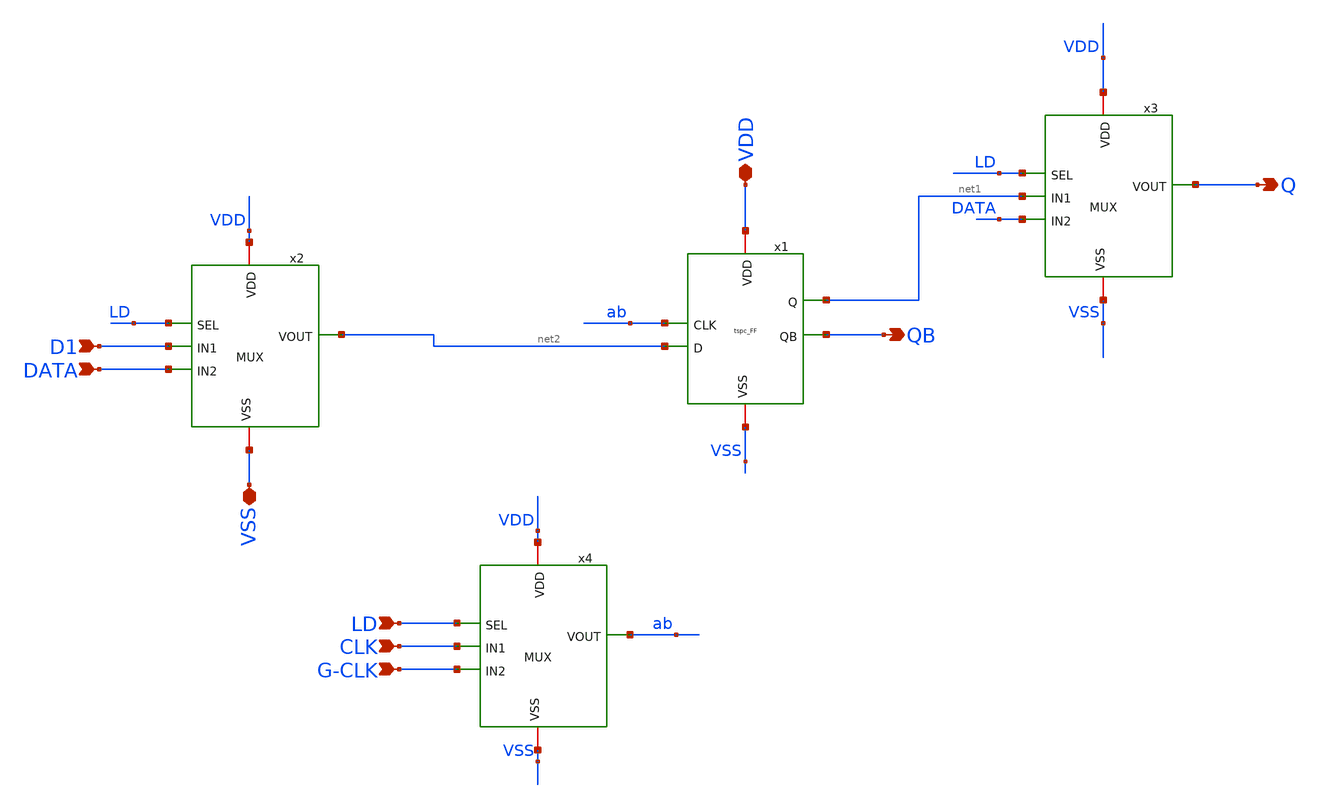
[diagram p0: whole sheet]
** sch_path: PLL-main/schematic/xschem/MOD_DFF_latest.sch
**.subckt MOD_DFF_latest VDD LD VSS D1 CLK G-CLK Q QB DATA
*.iopin VDD
*.ipin LD
*.iopin VSS
*.ipin D1
*.ipin CLK
*.ipin G-CLK
*.opin Q
*.opin QB
*.ipin DATA
x1 VDD QB net1 ab net2 VSS tspc_FF
x2 VDD LD D1 net2 VSS DATA MUX
x3 VDD LD net1 Q VSS DATA MUX
x4 VDD LD CLK ab VSS G-CLK MUX
**.ends

* expanding   symbol:  tspc_FF.sym # of pins=6
** sym_path: tspc_FF.sym
** sch_path: tspc_FF.sch
.subckt tspc_FF VDD QB Q CLK D VSS
*.ipin D
*.ipin CLK
*.iopin VDD
*.iopin VSS
*.opin QB
*.opin Q
XM1 net1 D VSS VSS nfet_03v3 L=0.56u W=1.12u nf=1 ad='int((nf+1)/2) * W/nf * 0.18u' as='int((nf+2)/2) * W/nf * 0.18u'
+ pd='2*int((nf+1)/2) * (W/nf + 0.18u)' ps='2*int((nf+2)/2) * (W/nf + 0.18u)' nrd='0.18u / W' nrs='0.18u / W'
+ sa=0 sb=0 sd=0 m=1
XM2 net1 CLK net2 VDD pfet_03v3 L=0.56u W=4.48u nf=1 ad='int((nf+1)/2) * W/nf * 0.18u' as='int((nf+2)/2) * W/nf * 0.18u'
+ pd='2*int((nf+1)/2) * (W/nf + 0.18u)' ps='2*int((nf+2)/2) * (W/nf + 0.18u)' nrd='0.18u / W' nrs='0.18u / W'
+ sa=0 sb=0 sd=0 m=1
XM3 net2 D VDD VDD pfet_03v3 L=0.56u W=4.48u nf=1 ad='int((nf+1)/2) * W/nf * 0.18u' as='int((nf+2)/2) * W/nf * 0.18u'
+ pd='2*int((nf+1)/2) * (W/nf + 0.18u)' ps='2*int((nf+2)/2) * (W/nf + 0.18u)' nrd='0.18u / W' nrs='0.18u / W'
+ sa=0 sb=0 sd=0 m=1
XM4 net3 CLK VDD VDD pfet_03v3 L=0.56u W=2.24u nf=1 ad='int((nf+1)/2) * W/nf * 0.18u' as='int((nf+2)/2) * W/nf * 0.18u'
+ pd='2*int((nf+1)/2) * (W/nf + 0.18u)' ps='2*int((nf+2)/2) * (W/nf + 0.18u)' nrd='0.18u / W' nrs='0.18u / W'
+ sa=0 sb=0 sd=0 m=1
XM5 net3 net1 net4 VSS nfet_03v3 L=0.56u W=2.24u nf=1 ad='int((nf+1)/2) * W/nf * 0.18u' as='int((nf+2)/2) * W/nf * 0.18u'
+ pd='2*int((nf+1)/2) * (W/nf + 0.18u)' ps='2*int((nf+2)/2) * (W/nf + 0.18u)' nrd='0.18u / W' nrs='0.18u / W'
+ sa=0 sb=0 sd=0 m=1
XM6 net4 CLK VSS VSS nfet_03v3 L=0.56u W=2.24u nf=1 ad='int((nf+1)/2) * W/nf * 0.18u' as='int((nf+2)/2) * W/nf * 0.18u'
+ pd='2*int((nf+1)/2) * (W/nf + 0.18u)' ps='2*int((nf+2)/2) * (W/nf + 0.18u)' nrd='0.18u / W' nrs='0.18u / W'
+ sa=0 sb=0 sd=0 m=1
XM7 QB net3 VDD VDD pfet_03v3 L=0.56u W=2.24u nf=1 ad='int((nf+1)/2) * W/nf * 0.18u' as='int((nf+2)/2) * W/nf * 0.18u'
+ pd='2*int((nf+1)/2) * (W/nf + 0.18u)' ps='2*int((nf+2)/2) * (W/nf + 0.18u)' nrd='0.18u / W' nrs='0.18u / W'
+ sa=0 sb=0 sd=0 m=1
XM8 QB CLK net5 VSS nfet_03v3 L=0.56u W=2.24u nf=1 ad='int((nf+1)/2) * W/nf * 0.18u' as='int((nf+2)/2) * W/nf * 0.18u'
+ pd='2*int((nf+1)/2) * (W/nf + 0.18u)' ps='2*int((nf+2)/2) * (W/nf + 0.18u)' nrd='0.18u / W' nrs='0.18u / W'
+ sa=0 sb=0 sd=0 m=1
XM9 net5 net3 VSS VSS nfet_03v3 L=0.56u W=2.24u nf=1 ad='int((nf+1)/2) * W/nf * 0.18u' as='int((nf+2)/2) * W/nf * 0.18u'
+ pd='2*int((nf+1)/2) * (W/nf + 0.18u)' ps='2*int((nf+2)/2) * (W/nf + 0.18u)' nrd='0.18u / W' nrs='0.18u / W'
+ sa=0 sb=0 sd=0 m=1
XM10 Q QB VDD VDD pfet_03v3 L=0.56u W=2.24u nf=1 ad='int((nf+1)/2) * W/nf * 0.18u' as='int((nf+2)/2) * W/nf * 0.18u'
+ pd='2*int((nf+1)/2) * (W/nf + 0.18u)' ps='2*int((nf+2)/2) * (W/nf + 0.18u)' nrd='0.18u / W' nrs='0.18u / W'
+ sa=0 sb=0 sd=0 m=1
XM11 Q QB VSS VSS nfet_03v3 L=0.56u W=1.12u nf=1 ad='int((nf+1)/2) * W/nf * 0.18u' as='int((nf+2)/2) * W/nf * 0.18u'
+ pd='2*int((nf+1)/2) * (W/nf + 0.18u)' ps='2*int((nf+2)/2) * (W/nf + 0.18u)' nrd='0.18u / W' nrs='0.18u / W'
+ sa=0 sb=0 sd=0 m=1
.ends


* expanding   symbol:  MUX.sym # of pins=6
** sym_path: MUX.sym
** sch_path: MUX.sch
.subckt MUX VDD SEL IN1 VOUT VSS IN2
*.ipin SEL
*.ipin IN1
*.ipin IN2
*.opin VOUT
*.iopin VDD
*.iopin VSS
x2 VDD net3 net1 IN1 VSS AND
x3 VDD net2 SEL IN2 VSS AND
XM4 net1 SEL VDD VDD pfet_03v3 L=0.56u W=6.72u nf=1 ad='int((nf+1)/2) * W/nf * 0.18u' as='int((nf+2)/2) * W/nf * 0.18u'
+ pd='2*int((nf+1)/2) * (W/nf + 0.18u)' ps='2*int((nf+2)/2) * (W/nf + 0.18u)' nrd='0.18u / W' nrs='0.18u / W'
+ sa=0 sb=0 sd=0 m=1
XM5 net1 SEL VSS VSS nfet_03v3 L=0.56u W=3.36u nf=1 ad='int((nf+1)/2) * W/nf * 0.18u' as='int((nf+2)/2) * W/nf * 0.18u'
+ pd='2*int((nf+1)/2) * (W/nf + 0.18u)' ps='2*int((nf+2)/2) * (W/nf + 0.18u)' nrd='0.18u / W' nrs='0.18u / W'
+ sa=0 sb=0 sd=0 m=1
x1 VDD net3 net2 VOUT VSS OR
.ends


* expanding   symbol:  AND.sym # of pins=5
** sym_path: AND.sym
** sch_path: AND.sch
.subckt AND VDD VOUT A B VSS
*.iopin VDD
*.iopin VSS
*.ipin A
*.ipin B
*.opin VOUT
XM1 net1 A net2 VSS nfet_03v3 L=0.56u W=2.24u nf=1 ad='int((nf+1)/2) * W/nf * 0.18u' as='int((nf+2)/2) * W/nf * 0.18u'
+ pd='2*int((nf+1)/2) * (W/nf + 0.18u)' ps='2*int((nf+2)/2) * (W/nf + 0.18u)' nrd='0.18u / W' nrs='0.18u / W'
+ sa=0 sb=0 sd=0 m=1
XM2 net1 A VDD VDD pfet_03v3 L=0.56u W=2.24u nf=1 ad='int((nf+1)/2) * W/nf * 0.18u' as='int((nf+2)/2) * W/nf * 0.18u'
+ pd='2*int((nf+1)/2) * (W/nf + 0.18u)' ps='2*int((nf+2)/2) * (W/nf + 0.18u)' nrd='0.18u / W' nrs='0.18u / W'
+ sa=0 sb=0 sd=0 m=1
XM3 net1 B VDD VDD pfet_03v3 L=0.56u W=2.24u nf=1 ad='int((nf+1)/2) * W/nf * 0.18u' as='int((nf+2)/2) * W/nf * 0.18u'
+ pd='2*int((nf+1)/2) * (W/nf + 0.18u)' ps='2*int((nf+2)/2) * (W/nf + 0.18u)' nrd='0.18u / W' nrs='0.18u / W'
+ sa=0 sb=0 sd=0 m=1
XM4 net2 B VSS VSS nfet_03v3 L=0.56u W=2.24u nf=1 ad='int((nf+1)/2) * W/nf * 0.18u' as='int((nf+2)/2) * W/nf * 0.18u'
+ pd='2*int((nf+1)/2) * (W/nf + 0.18u)' ps='2*int((nf+2)/2) * (W/nf + 0.18u)' nrd='0.18u / W' nrs='0.18u / W'
+ sa=0 sb=0 sd=0 m=1
XM5 VOUT net1 VDD VDD pfet_03v3 L=0.56u W=2.24u nf=1 ad='int((nf+1)/2) * W/nf * 0.18u' as='int((nf+2)/2) * W/nf * 0.18u'
+ pd='2*int((nf+1)/2) * (W/nf + 0.18u)' ps='2*int((nf+2)/2) * (W/nf + 0.18u)' nrd='0.18u / W' nrs='0.18u / W'
+ sa=0 sb=0 sd=0 m=1
XM6 VOUT net1 VSS VSS nfet_03v3 L=0.56u W=1.12u nf=1 ad='int((nf+1)/2) * W/nf * 0.18u' as='int((nf+2)/2) * W/nf * 0.18u'
+ pd='2*int((nf+1)/2) * (W/nf + 0.18u)' ps='2*int((nf+2)/2) * (W/nf + 0.18u)' nrd='0.18u / W' nrs='0.18u / W'
+ sa=0 sb=0 sd=0 m=1
.ends


* expanding   symbol:  OR.sym # of pins=5
** sym_path: PLL-main/schematic/xschem/OR.sym
** sch_path: PLL-main/schematic/xschem/OR.sch
.subckt OR VDD A B VOUT VSS
*.iopin VSS
*.iopin VDD
*.ipin A
*.ipin B
*.opin VOUT
XM1 net1 A VSS VSS nfet_03v3 L=0.56u W=1.12u nf=1 ad='int((nf+1)/2) * W/nf * 0.18u' as='int((nf+2)/2) * W/nf * 0.18u'
+ pd='2*int((nf+1)/2) * (W/nf + 0.18u)' ps='2*int((nf+2)/2) * (W/nf + 0.18u)' nrd='0.18u / W' nrs='0.18u / W'
+ sa=0 sb=0 sd=0 m=1
XM2 net1 B net2 VDD pfet_03v3 L=0.56u W=4.48u nf=1 ad='int((nf+1)/2) * W/nf * 0.18u' as='int((nf+2)/2) * W/nf * 0.18u'
+ pd='2*int((nf+1)/2) * (W/nf + 0.18u)' ps='2*int((nf+2)/2) * (W/nf + 0.18u)' nrd='0.18u / W' nrs='0.18u / W'
+ sa=0 sb=0 sd=0 m=1
XM3 net1 B VSS VSS nfet_03v3 L=0.56u W=1.12u nf=1 ad='int((nf+1)/2) * W/nf * 0.18u' as='int((nf+2)/2) * W/nf * 0.18u'
+ pd='2*int((nf+1)/2) * (W/nf + 0.18u)' ps='2*int((nf+2)/2) * (W/nf + 0.18u)' nrd='0.18u / W' nrs='0.18u / W'
+ sa=0 sb=0 sd=0 m=1
XM6 net2 A VDD VDD pfet_03v3 L=0.56u W=4.48u nf=1 ad='int((nf+1)/2) * W/nf * 0.18u' as='int((nf+2)/2) * W/nf * 0.18u'
+ pd='2*int((nf+1)/2) * (W/nf + 0.18u)' ps='2*int((nf+2)/2) * (W/nf + 0.18u)' nrd='0.18u / W' nrs='0.18u / W'
+ sa=0 sb=0 sd=0 m=1
XM4 VOUT net1 VDD VDD pfet_03v3 L=0.56u W=2.24u nf=1 ad='int((nf+1)/2) * W/nf * 0.18u' as='int((nf+2)/2) * W/nf * 0.18u'
+ pd='2*int((nf+1)/2) * (W/nf + 0.18u)' ps='2*int((nf+2)/2) * (W/nf + 0.18u)' nrd='0.18u / W' nrs='0.18u / W'
+ sa=0 sb=0 sd=0 m=1
XM5 VOUT net1 VSS VSS nfet_03v3 L=0.56u W=1.12u nf=1 ad='int((nf+1)/2) * W/nf * 0.18u' as='int((nf+2)/2) * W/nf * 0.18u'
+ pd='2*int((nf+1)/2) * (W/nf + 0.18u)' ps='2*int((nf+2)/2) * (W/nf + 0.18u)' nrd='0.18u / W' nrs='0.18u / W'
+ sa=0 sb=0 sd=0 m=1
.ends

.end
